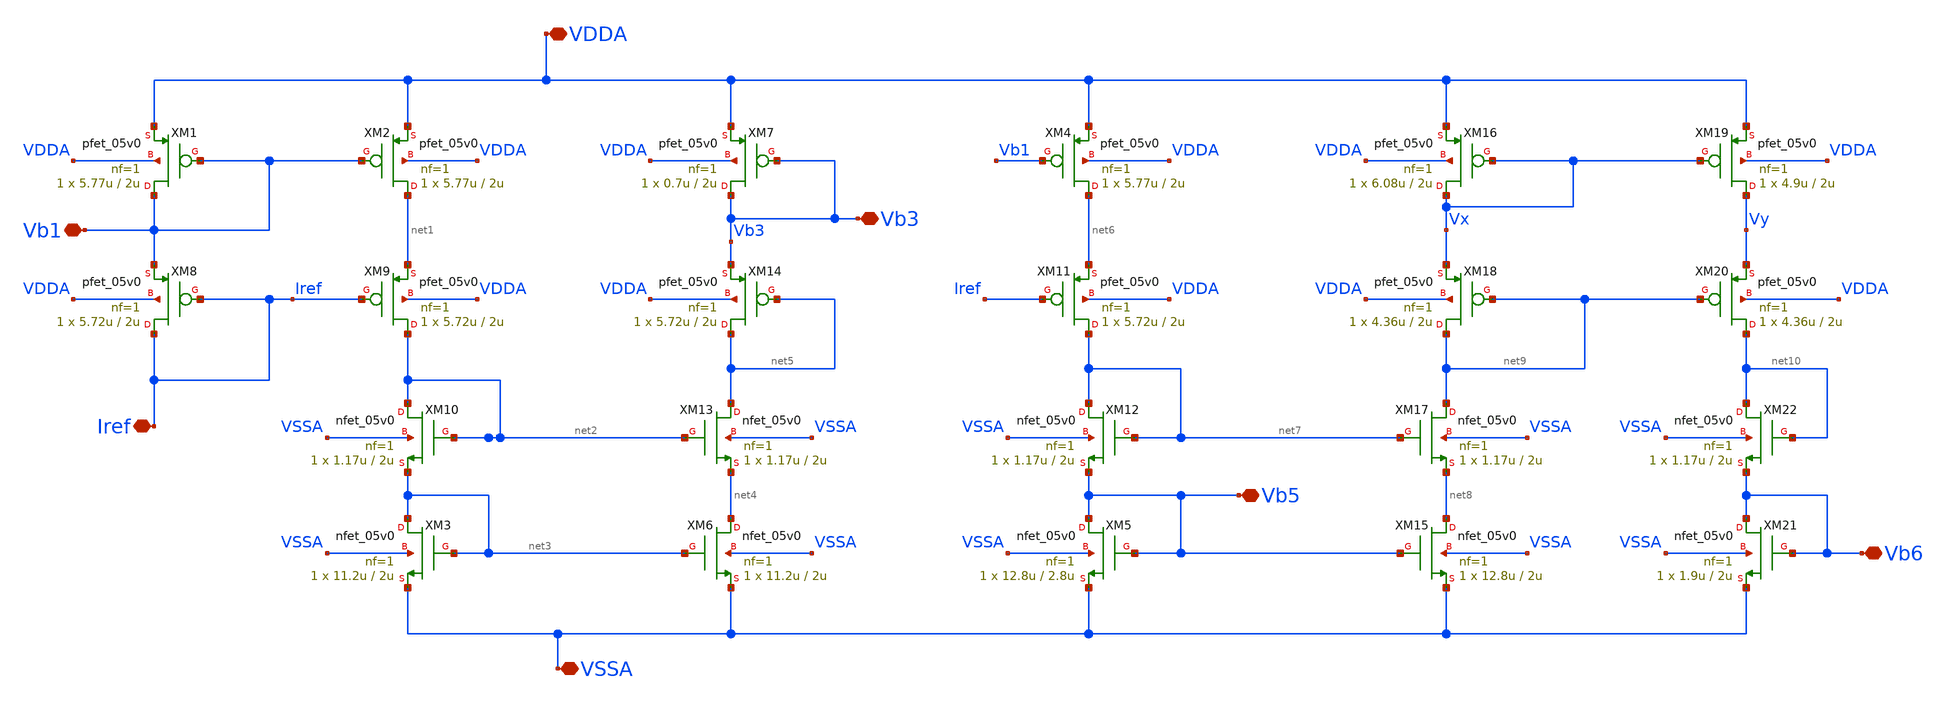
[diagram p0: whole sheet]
** sch_path: Folded_cascode/schematic/bias_circuit.sch
**.subckt bias_circuit VDDA VSSA Vb1 Vb5 Iref Vb3 Vb6
*.iopin VDDA
*.iopin VSSA
*.iopin Vb1
*.iopin Vb5
*.iopin Iref
*.iopin Vb3
*.iopin Vb6
XM1 Vb1 Vb1 VDDA VDDA pfet_05v0 L=2u W=5.77u nf=1 ad='int((nf+1)/2) * W/nf * 0.18u' as='int((nf+2)/2) * W/nf * 0.18u'
+ pd='2*int((nf+1)/2) * (W/nf + 0.18u)' ps='2*int((nf+2)/2) * (W/nf + 0.18u)' nrd='0.18u / W' nrs='0.18u / W'
+ sa=0 sb=0 sd=0 m=1
XM2 net1 Vb1 VDDA VDDA pfet_05v0 L=2u W=5.77u nf=1 ad='int((nf+1)/2) * W/nf * 0.18u' as='int((nf+2)/2) * W/nf * 0.18u'
+ pd='2*int((nf+1)/2) * (W/nf + 0.18u)' ps='2*int((nf+2)/2) * (W/nf + 0.18u)' nrd='0.18u / W' nrs='0.18u / W'
+ sa=0 sb=0 sd=0 m=1
XM3 net3 net3 VSSA VSSA nfet_05v0 L=2u W=11.2u nf=1 ad='int((nf+1)/2) * W/nf * 0.18u' as='int((nf+2)/2) * W/nf * 0.18u'
+ pd='2*int((nf+1)/2) * (W/nf + 0.18u)' ps='2*int((nf+2)/2) * (W/nf + 0.18u)' nrd='0.18u / W' nrs='0.18u / W'
+ sa=0 sb=0 sd=0 m=1
XM4 net6 Vb1 VDDA VDDA pfet_05v0 L=2u W=5.77u nf=1 ad='int((nf+1)/2) * W/nf * 0.18u' as='int((nf+2)/2) * W/nf * 0.18u'
+ pd='2*int((nf+1)/2) * (W/nf + 0.18u)' ps='2*int((nf+2)/2) * (W/nf + 0.18u)' nrd='0.18u / W' nrs='0.18u / W'
+ sa=0 sb=0 sd=0 m=1
XM5 Vb5 Vb5 VSSA VSSA nfet_05v0 L=2.8u W=12.8u nf=1 ad='int((nf+1)/2) * W/nf * 0.18u' as='int((nf+2)/2) * W/nf * 0.18u'
+ pd='2*int((nf+1)/2) * (W/nf + 0.18u)' ps='2*int((nf+2)/2) * (W/nf + 0.18u)' nrd='0.18u / W' nrs='0.18u / W'
+ sa=0 sb=0 sd=0 m=1
XM6 net4 net3 VSSA VSSA nfet_05v0 L=2u W=11.2u nf=1 ad='int((nf+1)/2) * W/nf * 0.18u' as='int((nf+2)/2) * W/nf * 0.18u'
+ pd='2*int((nf+1)/2) * (W/nf + 0.18u)' ps='2*int((nf+2)/2) * (W/nf + 0.18u)' nrd='0.18u / W' nrs='0.18u / W'
+ sa=0 sb=0 sd=0 m=1
XM7 Vb3 Vb3 VDDA VDDA pfet_05v0 L=2u W=0.7u nf=1 ad='int((nf+1)/2) * W/nf * 0.18u' as='int((nf+2)/2) * W/nf * 0.18u'
+ pd='2*int((nf+1)/2) * (W/nf + 0.18u)' ps='2*int((nf+2)/2) * (W/nf + 0.18u)' nrd='0.18u / W' nrs='0.18u / W'
+ sa=0 sb=0 sd=0 m=1
XM8 Iref Iref Vb1 VDDA pfet_05v0 L=2u W=5.72u nf=1 ad='int((nf+1)/2) * W/nf * 0.18u' as='int((nf+2)/2) * W/nf * 0.18u'
+ pd='2*int((nf+1)/2) * (W/nf + 0.18u)' ps='2*int((nf+2)/2) * (W/nf + 0.18u)' nrd='0.18u / W' nrs='0.18u / W'
+ sa=0 sb=0 sd=0 m=1
XM9 net2 Iref net1 VDDA pfet_05v0 L=2u W=5.72u nf=1 ad='int((nf+1)/2) * W/nf * 0.18u' as='int((nf+2)/2) * W/nf * 0.18u'
+ pd='2*int((nf+1)/2) * (W/nf + 0.18u)' ps='2*int((nf+2)/2) * (W/nf + 0.18u)' nrd='0.18u / W' nrs='0.18u / W'
+ sa=0 sb=0 sd=0 m=1
XM10 net2 net2 net3 VSSA nfet_05v0 L=2u W=1.17u nf=1 ad='int((nf+1)/2) * W/nf * 0.18u' as='int((nf+2)/2) * W/nf * 0.18u'
+ pd='2*int((nf+1)/2) * (W/nf + 0.18u)' ps='2*int((nf+2)/2) * (W/nf + 0.18u)' nrd='0.18u / W' nrs='0.18u / W'
+ sa=0 sb=0 sd=0 m=1
XM11 net7 Iref net6 VDDA pfet_05v0 L=2u W=5.72u nf=1 ad='int((nf+1)/2) * W/nf * 0.18u' as='int((nf+2)/2) * W/nf * 0.18u'
+ pd='2*int((nf+1)/2) * (W/nf + 0.18u)' ps='2*int((nf+2)/2) * (W/nf + 0.18u)' nrd='0.18u / W' nrs='0.18u / W'
+ sa=0 sb=0 sd=0 m=1
XM12 net7 net7 Vb5 VSSA nfet_05v0 L=2u W=1.17u nf=1 ad='int((nf+1)/2) * W/nf * 0.18u' as='int((nf+2)/2) * W/nf * 0.18u'
+ pd='2*int((nf+1)/2) * (W/nf + 0.18u)' ps='2*int((nf+2)/2) * (W/nf + 0.18u)' nrd='0.18u / W' nrs='0.18u / W'
+ sa=0 sb=0 sd=0 m=1
XM13 net5 net2 net4 VSSA nfet_05v0 L=2u W=1.17u nf=1 ad='int((nf+1)/2) * W/nf * 0.18u' as='int((nf+2)/2) * W/nf * 0.18u'
+ pd='2*int((nf+1)/2) * (W/nf + 0.18u)' ps='2*int((nf+2)/2) * (W/nf + 0.18u)' nrd='0.18u / W' nrs='0.18u / W'
+ sa=0 sb=0 sd=0 m=1
XM14 net5 net5 Vb3 VDDA pfet_05v0 L=2u W=5.72u nf=1 ad='int((nf+1)/2) * W/nf * 0.18u' as='int((nf+2)/2) * W/nf * 0.18u'
+ pd='2*int((nf+1)/2) * (W/nf + 0.18u)' ps='2*int((nf+2)/2) * (W/nf + 0.18u)' nrd='0.18u / W' nrs='0.18u / W'
+ sa=0 sb=0 sd=0 m=1
XM15 net8 Vb5 VSSA VSSA nfet_05v0 L=2u W=12.8u nf=1 ad='int((nf+1)/2) * W/nf * 0.18u' as='int((nf+2)/2) * W/nf * 0.18u'
+ pd='2*int((nf+1)/2) * (W/nf + 0.18u)' ps='2*int((nf+2)/2) * (W/nf + 0.18u)' nrd='0.18u / W' nrs='0.18u / W'
+ sa=0 sb=0 sd=0 m=1
XM16 Vx Vx VDDA VDDA pfet_05v0 L=2u W=6.08u nf=1 ad='int((nf+1)/2) * W/nf * 0.18u' as='int((nf+2)/2) * W/nf * 0.18u'
+ pd='2*int((nf+1)/2) * (W/nf + 0.18u)' ps='2*int((nf+2)/2) * (W/nf + 0.18u)' nrd='0.18u / W' nrs='0.18u / W'
+ sa=0 sb=0 sd=0 m=1
XM18 net9 net9 Vx VDDA pfet_05v0 L=2u W=4.36u nf=1 ad='int((nf+1)/2) * W/nf * 0.18u' as='int((nf+2)/2) * W/nf * 0.18u'
+ pd='2*int((nf+1)/2) * (W/nf + 0.18u)' ps='2*int((nf+2)/2) * (W/nf + 0.18u)' nrd='0.18u / W' nrs='0.18u / W'
+ sa=0 sb=0 sd=0 m=1
XM19 Vy Vx VDDA VDDA pfet_05v0 L=2u W=4.9u nf=1 ad='int((nf+1)/2) * W/nf * 0.18u' as='int((nf+2)/2) * W/nf * 0.18u'
+ pd='2*int((nf+1)/2) * (W/nf + 0.18u)' ps='2*int((nf+2)/2) * (W/nf + 0.18u)' nrd='0.18u / W' nrs='0.18u / W'
+ sa=0 sb=0 sd=0 m=1
XM20 net10 net9 Vy VDDA pfet_05v0 L=2u W=4.36u nf=1 ad='int((nf+1)/2) * W/nf * 0.18u' as='int((nf+2)/2) * W/nf * 0.18u'
+ pd='2*int((nf+1)/2) * (W/nf + 0.18u)' ps='2*int((nf+2)/2) * (W/nf + 0.18u)' nrd='0.18u / W' nrs='0.18u / W'
+ sa=0 sb=0 sd=0 m=1
XM21 Vb6 Vb6 VSSA VSSA nfet_05v0 L=2u W=1.9u nf=1 ad='int((nf+1)/2) * W/nf * 0.18u' as='int((nf+2)/2) * W/nf * 0.18u'
+ pd='2*int((nf+1)/2) * (W/nf + 0.18u)' ps='2*int((nf+2)/2) * (W/nf + 0.18u)' nrd='0.18u / W' nrs='0.18u / W'
+ sa=0 sb=0 sd=0 m=1
XM22 net10 net10 Vb6 VSSA nfet_05v0 L=2u W=1.17u nf=1 ad='int((nf+1)/2) * W/nf * 0.18u' as='int((nf+2)/2) * W/nf * 0.18u'
+ pd='2*int((nf+1)/2) * (W/nf + 0.18u)' ps='2*int((nf+2)/2) * (W/nf + 0.18u)' nrd='0.18u / W' nrs='0.18u / W'
+ sa=0 sb=0 sd=0 m=1
XM17 net9 net7 net8 VSSA nfet_05v0 L=2u W=1.17u nf=1 ad='int((nf+1)/2) * W/nf * 0.18u' as='int((nf+2)/2) * W/nf * 0.18u'
+ pd='2*int((nf+1)/2) * (W/nf + 0.18u)' ps='2*int((nf+2)/2) * (W/nf + 0.18u)' nrd='0.18u / W' nrs='0.18u / W'
+ sa=0 sb=0 sd=0 m=1
**.ends
.end
